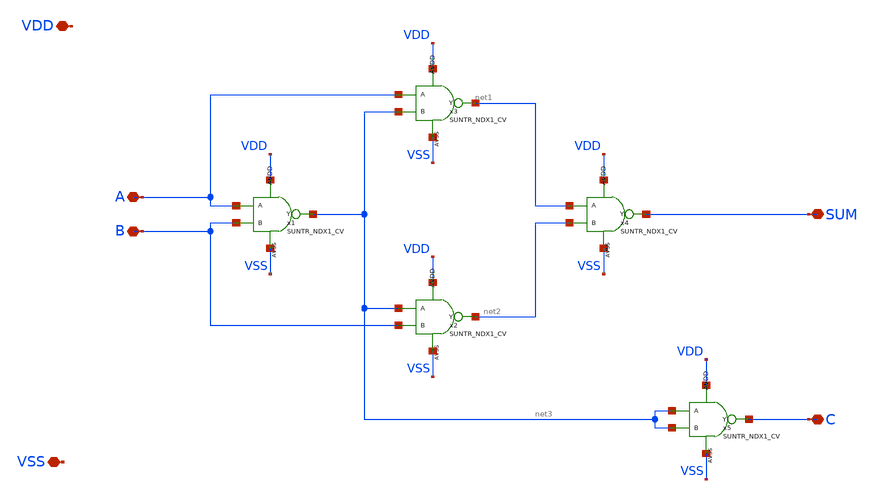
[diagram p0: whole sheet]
** sch_path: design/CNR_GR03_SKY130NM/HALF_ADDER.sch
**.subckt HALF_ADDER A B SUM C VDD VSS
*.iopin A
*.iopin B
*.iopin SUM
*.iopin C
*.iopin VDD
*.iopin VSS
x1 A B net3 VDD VSS SUNTR_NDX1_CV
x2 net3 B net2 VDD VSS SUNTR_NDX1_CV
x3 A net3 net1 VDD VSS SUNTR_NDX1_CV
x4 net1 net2 SUM VDD VSS SUNTR_NDX1_CV
x5 net3 net3 C VDD VSS SUNTR_NDX1_CV
**.ends
.end
